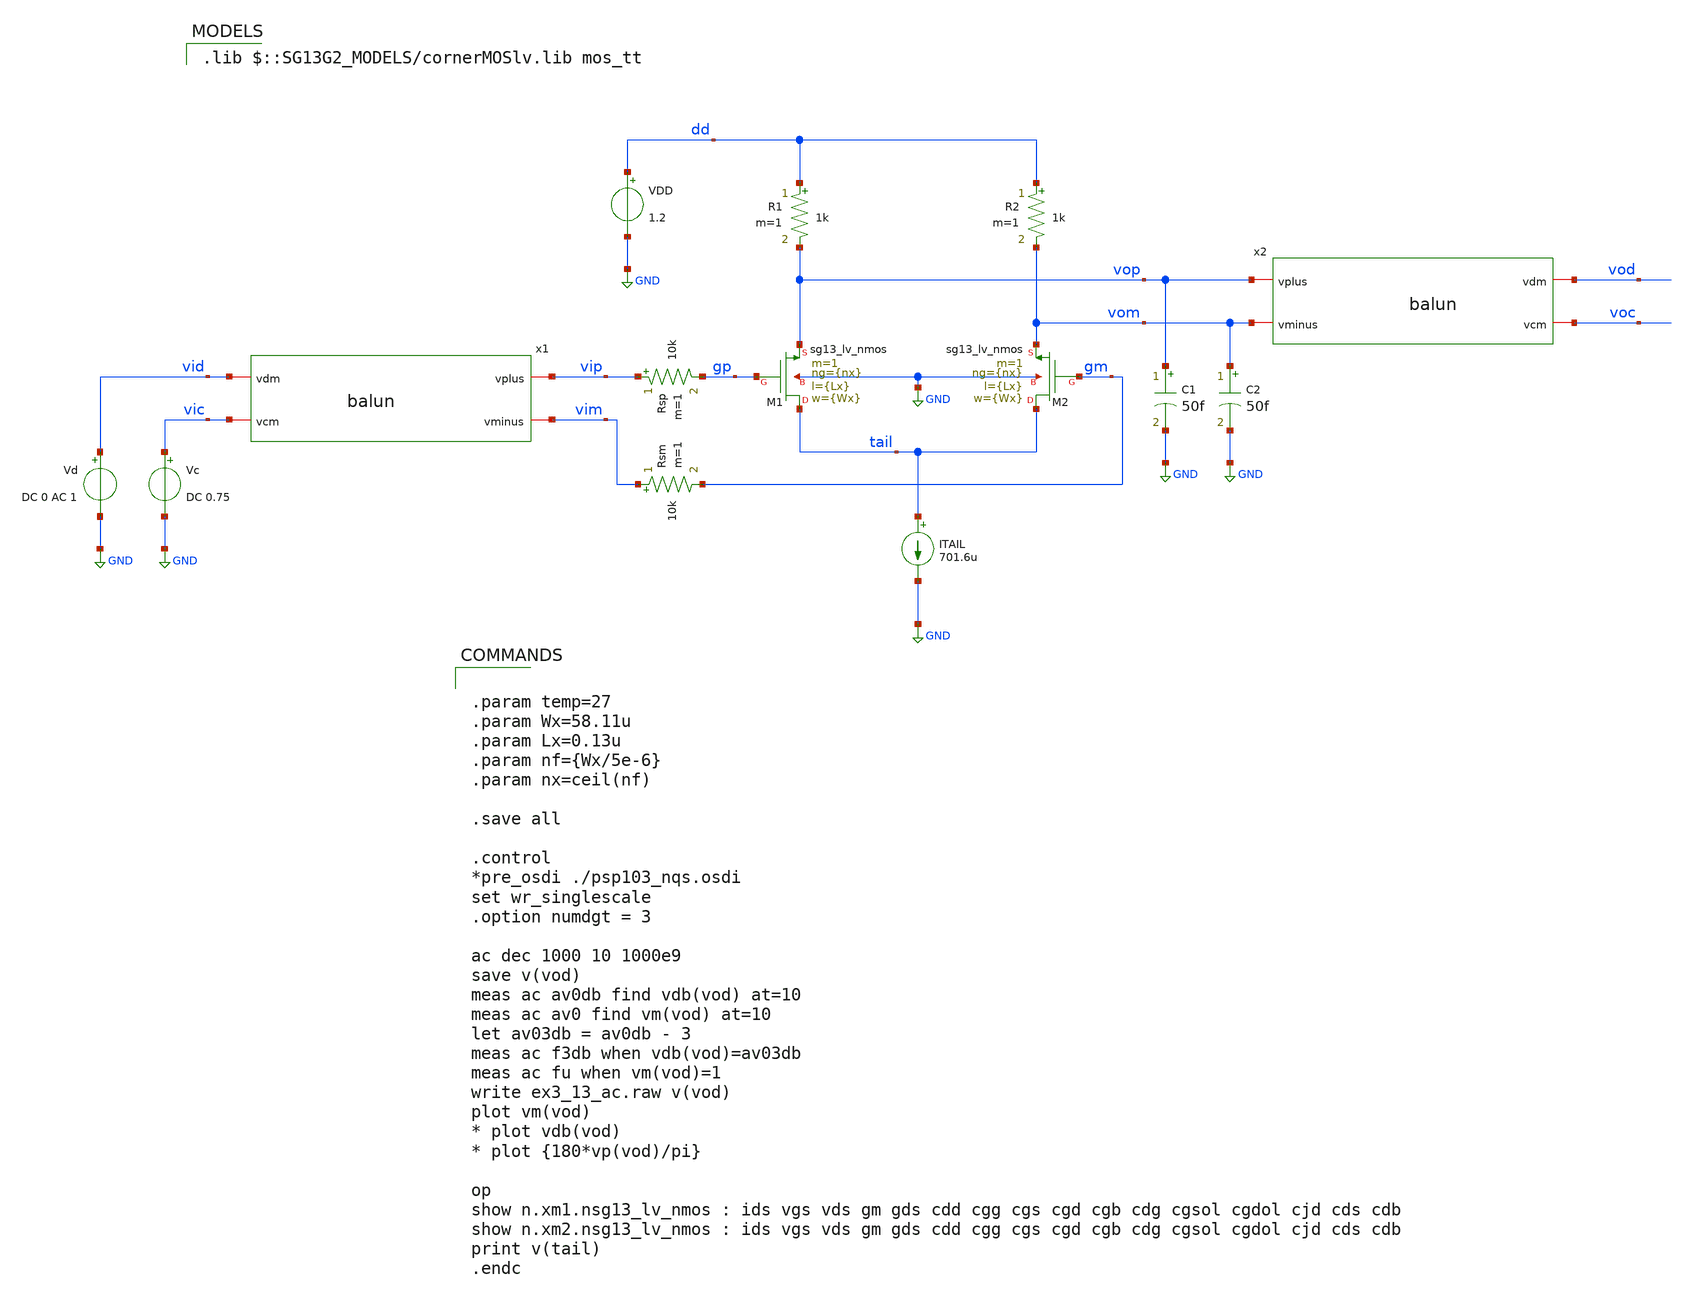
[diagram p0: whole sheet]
** sch_path: 03_design_examples/examples/src/ex3_13.sch
**.subckt ex3_13
XM1 tail gp vop GND sg13_lv_nmos w={Wx} l={Lx} ng={nx} m=1 mm_ok=1
XM2 tail gm vom GND sg13_lv_nmos w={Wx} l={Lx} ng={nx} m=1 mm_ok=1
ITAIL tail GND 701.6u
R2 dd vom 1k m=1
R1 dd vop 1k m=1
VDD dd GND 1.2
Vc vic GND DC 0.75
Vd vid GND DC 0 AC 1
C1 vop GND 50f m=1
C2 vom GND 50f m=1
Rsp vip gp 10k m=1
Rsm vim gm 10k m=1
x1 vid vic vip vim balun
x2 vod voc vop vom balun
**** begin user architecture code


.param temp=27
.param Wx=58.11u
.param Lx=0.13u
.param nf={Wx/5e-6}
.param nx=ceil(nf)

.save all

.control
*pre_osdi ./psp103_nqs.osdi
set wr_singlescale
.option numdgt = 3

ac dec 1000 10 1000e9
save v(vod)
meas ac av0db find vdb(vod) at=10
meas ac av0 find vm(vod) at=10
let av03db = av0db - 3
meas ac f3db when vdb(vod)=av03db
meas ac fu when vm(vod)=1
write ex3_13_ac.raw v(vod)
plot vm(vod)
* plot vdb(vod)
* plot {180*vp(vod)/pi}

op
show n.xm1.nsg13_lv_nmos : ids vgs vds gm gds cdd cgg cgs cgd cgb cdg cgsol cgdol cjd cds cdb
show n.xm2.nsg13_lv_nmos : ids vgs vds gm gds cdd cgg cgs cgd cgb cdg cgsol cgdol cjd cds cdb
print v(tail)
.endc


 .lib $::SG13G2_MODELS/cornerMOSlv.lib mos_tt

**** end user architecture code
**.ends

* expanding   symbol:  /foss/designs/gmid/balun.sym # of pins=4
** sym_path: 03_design_examples/examples/src/balun.sym
** sch_path: 03_design_examples/examples/src/balun.sch
.subckt balun vdm vcm vplus vminus
*.iopin vdm
*.iopin vcm
*.iopin vplus
*.iopin vminus
**** begin user architecture code


*Balun Circuit - by K. Kundert
e1 nodeA vcm vdm 0 0.5
v1 vplus nodeA 0
f1 vdm 0 v1 -0.5
r1 vdm 0 1G
e2 nodeB vminus vdm 0 0.5
v2 vcm nodeC 0
f2 vdm 0 v2 -0.5
r2 nodec nodeB 1u


**** end user architecture code
.ends

.GLOBAL GND
.end
